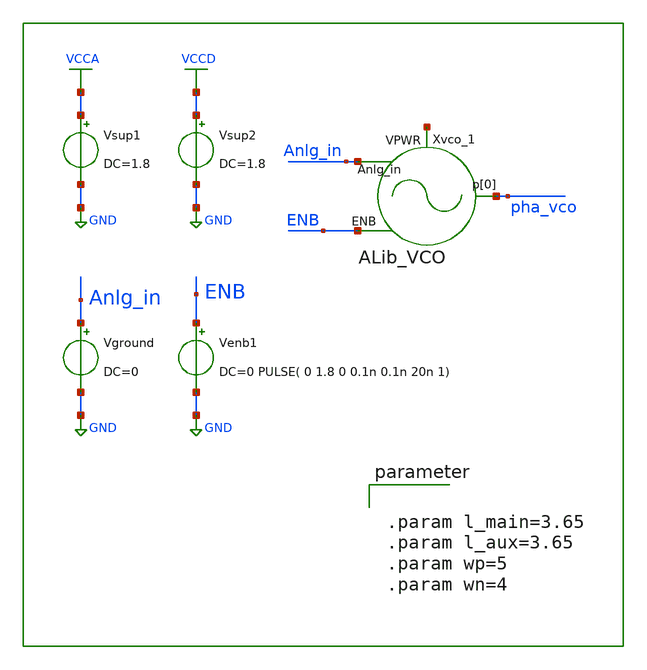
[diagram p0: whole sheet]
** sch_path: xschem/tb/VCO_tb.sch

.include $::SKYWATER_STDCELLS/sky130_fd_sc_hd.spice
.lib $::SKYWATER_MODELS/sky130.lib.spice tt

**.subckt VCO_tb
Vground Anlg_in GND DC=0
Venb1 ENB GND DC=0 PULSE( 0 1.8 0 0.1n 0.1n 20n 1)
Xvco_1 net1 pha_vco Anlg_in ENB ALib_VCO L12=0.15 Wp12=2.4 Wn12=1.2 L34=0.15 Wp34=1.2 Wn34=0.65
Vsup1 VCCA GND DC=1.8
Vsup2 VCCD GND DC=1.8
**** begin user architecture code


.param l_main=3.65
.param l_aux=3.65
.param wp=5
.param wn=4


**** end user architecture code
**.ends
.GLOBAL GND
.GLOBAL VCCA
.GLOBAL VCCD
**** begin user architecture code


.control
set nobreak
set num_threads=8
set test_mode = 1
* mode = 0: operation testing				1:  frequency extraction    2:  power consumption
if ($test_mode = 0)
    TRAN 1n 5u
    plot pha_vco
    MEAS TRAN prd TRIG pha_vco VAL=0.8 RISE=10 TARG pha_vco VAL=0.8 RISE=20
    let freq = 10/prd
    echo "frequency: "
    print freq
end
if ($test_mode = 1)
    let Vlow = 0
    let Vlimit = 1.01     $ set upper bound for sweeping
    let Vsweep = 0.01      $ set step size for sweeping
    let NoPoints=(Vlimit-Vlow)/Vsweep+2    $ set number of points for sweeping
    let freq =unitvec(NoPoints)
    let Vin  =unitvec(NoPoints)
    let Vin[0]=Vlow
    let ix=0
    while Vin[ix] < Vlimit
        alter Vground DC=Vin[ix]
        TRAN 0.4n 12u
        MEAS TRAN prd TRIG pha_vco VAL=0.8 RISE=10 TARG pha_vco VAL=0.8 RISE =20
        let freq[ix] = 10/prd
        let ix = ix+1
        Let Vin[ix] = Vin[ix-1]+Vsweep
    end
   print Vin freq > freq_ext.txt
end
if ($test_mode = 2)
    save "vdd" @Vsup[i] "p[0]"
    TRAN 0.1n 5u
    MEAS TRAN I_vco AVG @Vsup[i] FROM=3u TO=4u
    MEAS TRAN V_vco AVG vdd FROM=3u TO=4u
    let Power=I_vco*V_vco
    print Power
end
.endc


**** end user architecture code
.end
